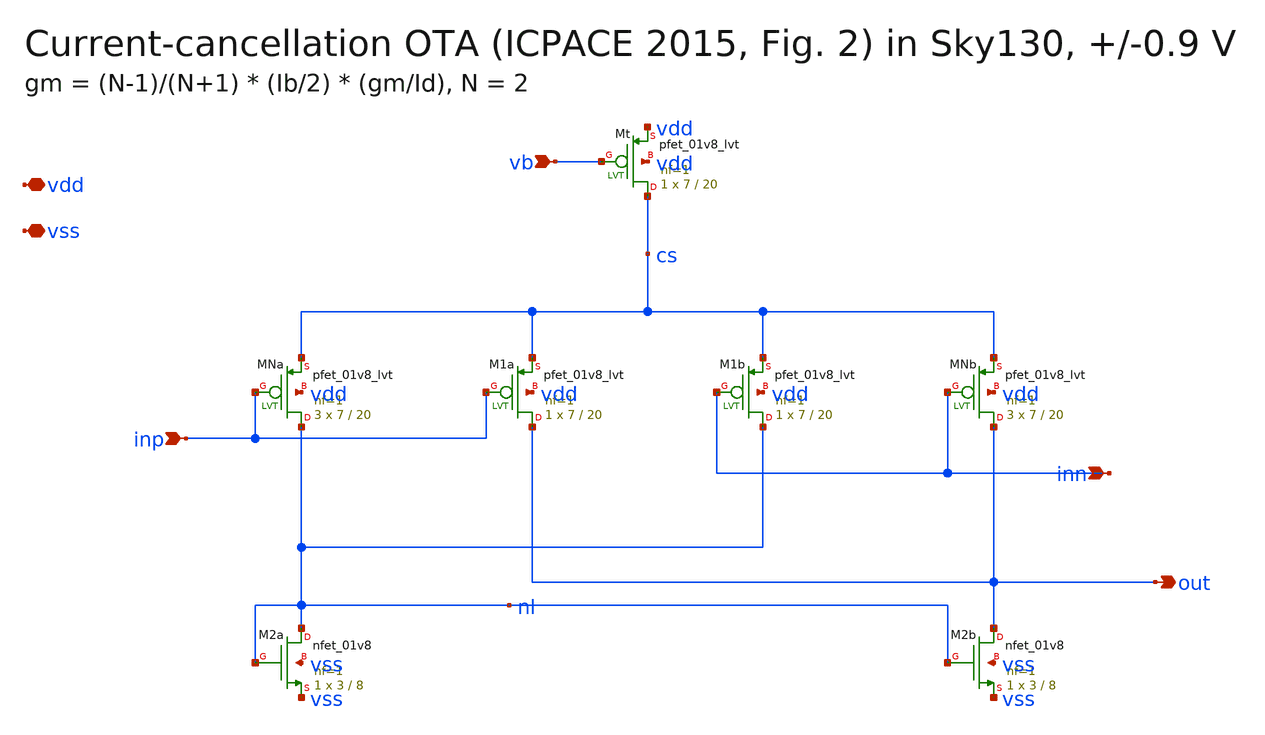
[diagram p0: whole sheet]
** sch_path: notch_ota_current_cancellation/schematics/ota_cc.sch
**.subckt ota_cc inp inn out vb vdd vss
*.ipin inp
*.ipin inn
*.opin out
*.ipin vb
*.iopin vdd
*.iopin vss
XMt cs vb vdd vdd sky130_fd_pr__pfet_01v8_lvt L=20 W=7 nf=1 ad='int((nf+1)/2) * W/nf * 0.29' as='int((nf+2)/2) * W/nf * 0.29'
+ pd='2*int((nf+1)/2) * (W/nf + 0.29)' ps='2*int((nf+2)/2) * (W/nf + 0.29)' nrd='0.29 / W' nrs='0.29 / W'
+ sa=0 sb=0 sd=0 mult=1 m=1
XMNa nl inp cs vdd sky130_fd_pr__pfet_01v8_lvt L=20 W=7 nf=1 ad='int((nf+1)/2) * W/nf * 0.29' as='int((nf+2)/2) * W/nf * 0.29'
+ pd='2*int((nf+1)/2) * (W/nf + 0.29)' ps='2*int((nf+2)/2) * (W/nf + 0.29)' nrd='0.29 / W' nrs='0.29 / W'
+ sa=0 sb=0 sd=0 mult=3 m=3
XM1a out inp cs vdd sky130_fd_pr__pfet_01v8_lvt L=20 W=7 nf=1 ad='int((nf+1)/2) * W/nf * 0.29' as='int((nf+2)/2) * W/nf * 0.29'
+ pd='2*int((nf+1)/2) * (W/nf + 0.29)' ps='2*int((nf+2)/2) * (W/nf + 0.29)' nrd='0.29 / W' nrs='0.29 / W'
+ sa=0 sb=0 sd=0 mult=1 m=1
XM1b nl inn cs vdd sky130_fd_pr__pfet_01v8_lvt L=20 W=7 nf=1 ad='int((nf+1)/2) * W/nf * 0.29' as='int((nf+2)/2) * W/nf * 0.29'
+ pd='2*int((nf+1)/2) * (W/nf + 0.29)' ps='2*int((nf+2)/2) * (W/nf + 0.29)' nrd='0.29 / W' nrs='0.29 / W'
+ sa=0 sb=0 sd=0 mult=1 m=1
XMNb out inn cs vdd sky130_fd_pr__pfet_01v8_lvt L=20 W=7 nf=1 ad='int((nf+1)/2) * W/nf * 0.29' as='int((nf+2)/2) * W/nf * 0.29'
+ pd='2*int((nf+1)/2) * (W/nf + 0.29)' ps='2*int((nf+2)/2) * (W/nf + 0.29)' nrd='0.29 / W' nrs='0.29 / W'
+ sa=0 sb=0 sd=0 mult=3 m=3
XM2a nl nl vss vss sky130_fd_pr__nfet_01v8 L=8 W=3 nf=1 ad='int((nf+1)/2) * W/nf * 0.29' as='int((nf+2)/2) * W/nf * 0.29'
+ pd='2*int((nf+1)/2) * (W/nf + 0.29)' ps='2*int((nf+2)/2) * (W/nf + 0.29)' nrd='0.29 / W' nrs='0.29 / W'
+ sa=0 sb=0 sd=0 mult=1 m=1
XM2b out nl vss vss sky130_fd_pr__nfet_01v8 L=8 W=3 nf=1 ad='int((nf+1)/2) * W/nf * 0.29' as='int((nf+2)/2) * W/nf * 0.29'
+ pd='2*int((nf+1)/2) * (W/nf + 0.29)' ps='2*int((nf+2)/2) * (W/nf + 0.29)' nrd='0.29 / W' nrs='0.29 / W'
+ sa=0 sb=0 sd=0 mult=1 m=1
**.ends
.end
